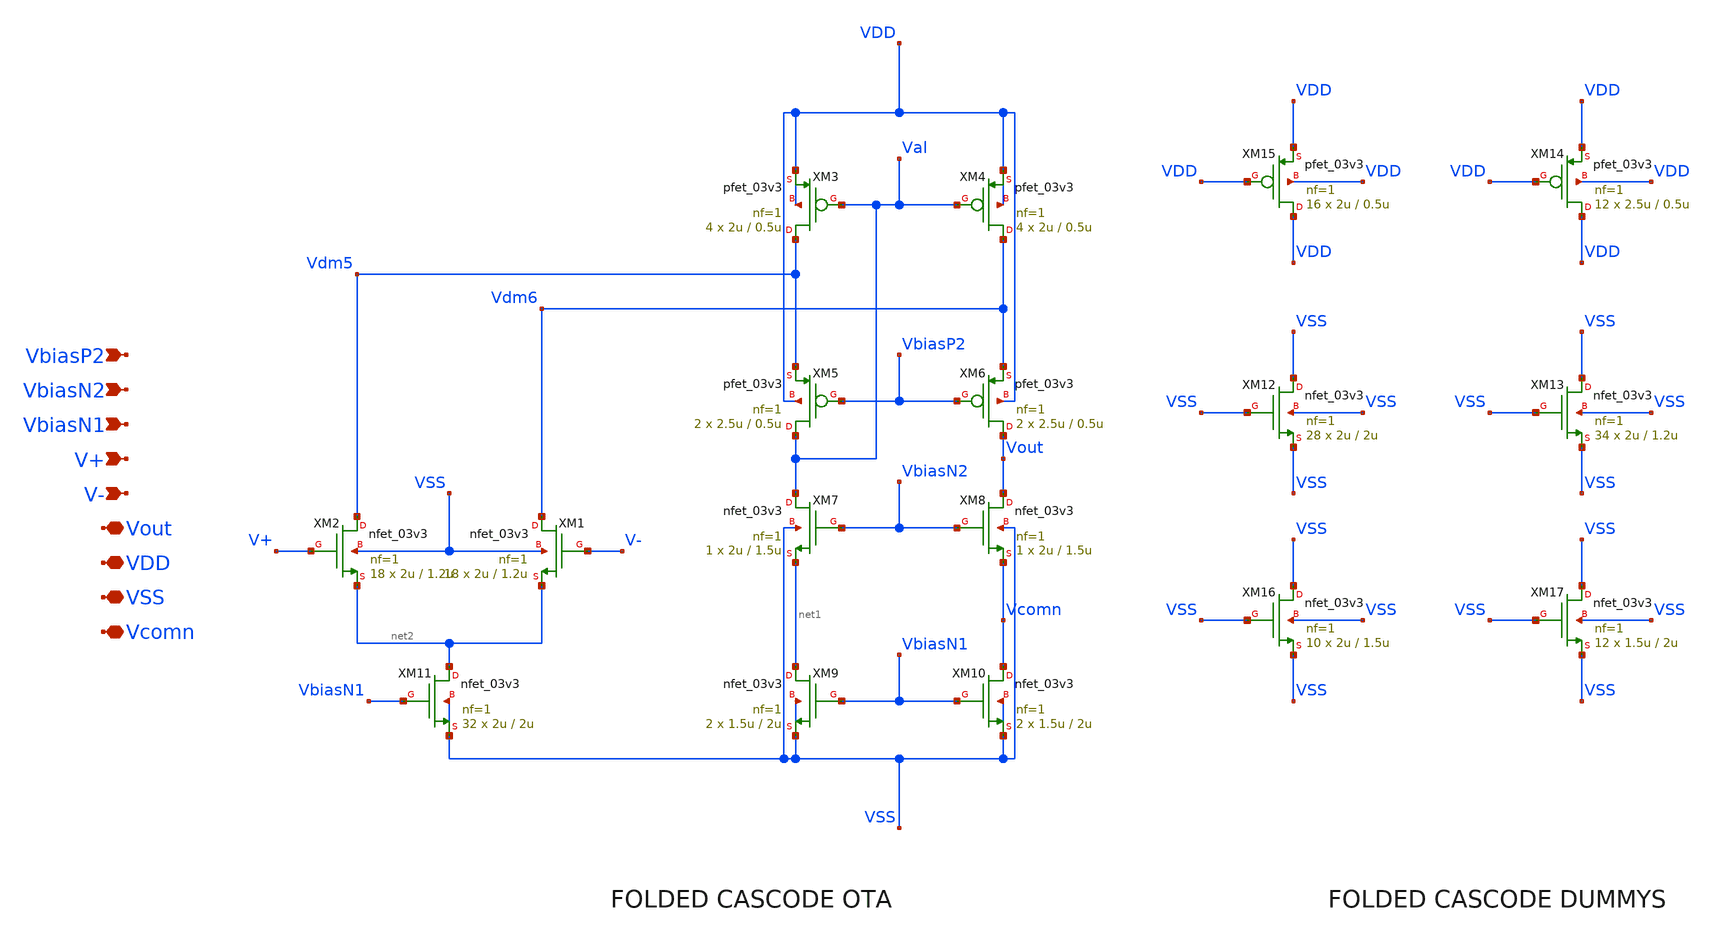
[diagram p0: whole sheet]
** sch_path: designs/gf180/error_amplifier_N_input_core_v3/xschem/error_amplifier_N_input_core_v3.sch
**.subckt error_amplifier_N_input_core_v3 VbiasN2 VDD VbiasP2 VbiasN1 V+ V- VSS Vcomn Vout
*.ipin VbiasN2
*.iopin VDD
*.ipin VbiasP2
*.ipin VbiasN1
*.ipin V+
*.ipin V-
*.iopin VSS
*.iopin Vcomn
*.iopin Vout
XM4 Vdm6 Val VDD VDD pfet_03v3 L=0.5u W=2u nf=1 ad='int((nf+1)/2) * W/nf * 0.18u' as='int((nf+2)/2) * W/nf * 0.18u'
+ pd='2*int((nf+1)/2) * (W/nf + 0.18u)' ps='2*int((nf+2)/2) * (W/nf + 0.18u)' nrd='0.18u / W' nrs='0.18u / W'
+ sa=0 sb=0 sd=0 m=4
XM3 Vdm5 Val VDD VDD pfet_03v3 L=0.5u W=2u nf=1 ad='int((nf+1)/2) * W/nf * 0.18u' as='int((nf+2)/2) * W/nf * 0.18u'
+ pd='2*int((nf+1)/2) * (W/nf + 0.18u)' ps='2*int((nf+2)/2) * (W/nf + 0.18u)' nrd='0.18u / W' nrs='0.18u / W'
+ sa=0 sb=0 sd=0 m=4
XM5 Val VbiasP2 Vdm5 VDD pfet_03v3 L=0.5u W=2.5u nf=1 ad='int((nf+1)/2) * W/nf * 0.18u' as='int((nf+2)/2) * W/nf * 0.18u'
+ pd='2*int((nf+1)/2) * (W/nf + 0.18u)' ps='2*int((nf+2)/2) * (W/nf + 0.18u)' nrd='0.18u / W' nrs='0.18u / W'
+ sa=0 sb=0 sd=0 m=2
XM6 Vout VbiasP2 Vdm6 VDD pfet_03v3 L=0.5u W=2.5u nf=1 ad='int((nf+1)/2) * W/nf * 0.18u' as='int((nf+2)/2) * W/nf * 0.18u'
+ pd='2*int((nf+1)/2) * (W/nf + 0.18u)' ps='2*int((nf+2)/2) * (W/nf + 0.18u)' nrd='0.18u / W' nrs='0.18u / W'
+ sa=0 sb=0 sd=0 m=2
XM9 net1 VbiasN1 VSS VSS nfet_03v3 L=2u W=1.5u nf=1 ad='int((nf+1)/2) * W/nf * 0.18u' as='int((nf+2)/2) * W/nf * 0.18u'
+ pd='2*int((nf+1)/2) * (W/nf + 0.18u)' ps='2*int((nf+2)/2) * (W/nf + 0.18u)' nrd='0.18u / W' nrs='0.18u / W'
+ sa=0 sb=0 sd=0 m=2
XM8 Vout VbiasN2 Vcomn VSS nfet_03v3 L=1.5u W=2u nf=1 ad='int((nf+1)/2) * W/nf * 0.18u' as='int((nf+2)/2) * W/nf * 0.18u'
+ pd='2*int((nf+1)/2) * (W/nf + 0.18u)' ps='2*int((nf+2)/2) * (W/nf + 0.18u)' nrd='0.18u / W' nrs='0.18u / W'
+ sa=0 sb=0 sd=0 m=1
XM7 Val VbiasN2 net1 VSS nfet_03v3 L=1.5u W=2u nf=1 ad='int((nf+1)/2) * W/nf * 0.18u' as='int((nf+2)/2) * W/nf * 0.18u'
+ pd='2*int((nf+1)/2) * (W/nf + 0.18u)' ps='2*int((nf+2)/2) * (W/nf + 0.18u)' nrd='0.18u / W' nrs='0.18u / W'
+ sa=0 sb=0 sd=0 m=1
XM10 Vcomn VbiasN1 VSS VSS nfet_03v3 L=2u W=1.5u nf=1 ad='int((nf+1)/2) * W/nf * 0.18u' as='int((nf+2)/2) * W/nf * 0.18u'
+ pd='2*int((nf+1)/2) * (W/nf + 0.18u)' ps='2*int((nf+2)/2) * (W/nf + 0.18u)' nrd='0.18u / W' nrs='0.18u / W'
+ sa=0 sb=0 sd=0 m=2
XM15 VDD VDD VDD VDD pfet_03v3 L=0.5u W=2u nf=1 ad='int((nf+1)/2) * W/nf * 0.18u' as='int((nf+2)/2) * W/nf * 0.18u'
+ pd='2*int((nf+1)/2) * (W/nf + 0.18u)' ps='2*int((nf+2)/2) * (W/nf + 0.18u)' nrd='0.18u / W' nrs='0.18u / W'
+ sa=0 sb=0 sd=0 m=16
XM13 VSS VSS VSS VSS nfet_03v3 L=1.2u W=2u nf=1 ad='int((nf+1)/2) * W/nf * 0.18u' as='int((nf+2)/2) * W/nf * 0.18u'
+ pd='2*int((nf+1)/2) * (W/nf + 0.18u)' ps='2*int((nf+2)/2) * (W/nf + 0.18u)' nrd='0.18u / W' nrs='0.18u / W'
+ sa=0 sb=0 sd=0 m=34
XM12 VSS VSS VSS VSS nfet_03v3 L=2u W=2u nf=1 ad='int((nf+1)/2) * W/nf * 0.18u' as='int((nf+2)/2) * W/nf * 0.18u'
+ pd='2*int((nf+1)/2) * (W/nf + 0.18u)' ps='2*int((nf+2)/2) * (W/nf + 0.18u)' nrd='0.18u / W' nrs='0.18u / W'
+ sa=0 sb=0 sd=0 m=28
XM1 Vdm6 V- net2 VSS nfet_03v3 L=1.2u W=2u nf=1 ad='int((nf+1)/2) * W/nf * 0.18u' as='int((nf+2)/2) * W/nf * 0.18u'
+ pd='2*int((nf+1)/2) * (W/nf + 0.18u)' ps='2*int((nf+2)/2) * (W/nf + 0.18u)' nrd='0.18u / W' nrs='0.18u / W'
+ sa=0 sb=0 sd=0 m=18
XM2 Vdm5 V+ net2 VSS nfet_03v3 L=1.2u W=2u nf=1 ad='int((nf+1)/2) * W/nf * 0.18u' as='int((nf+2)/2) * W/nf * 0.18u'
+ pd='2*int((nf+1)/2) * (W/nf + 0.18u)' ps='2*int((nf+2)/2) * (W/nf + 0.18u)' nrd='0.18u / W' nrs='0.18u / W'
+ sa=0 sb=0 sd=0 m=18
XM11 net2 VbiasN1 VSS VSS nfet_03v3 L=2u W=2u nf=1 ad='int((nf+1)/2) * W/nf * 0.18u' as='int((nf+2)/2) * W/nf * 0.18u'
+ pd='2*int((nf+1)/2) * (W/nf + 0.18u)' ps='2*int((nf+2)/2) * (W/nf + 0.18u)' nrd='0.18u / W' nrs='0.18u / W'
+ sa=0 sb=0 sd=0 m=32
XM14 VDD VDD VDD VDD pfet_03v3 L=0.5u W=2.5u nf=1 ad='int((nf+1)/2) * W/nf * 0.18u' as='int((nf+2)/2) * W/nf * 0.18u'
+ pd='2*int((nf+1)/2) * (W/nf + 0.18u)' ps='2*int((nf+2)/2) * (W/nf + 0.18u)' nrd='0.18u / W' nrs='0.18u / W'
+ sa=0 sb=0 sd=0 m=12
XM16 VSS VSS VSS VSS nfet_03v3 L=1.5u W=2u nf=1 ad='int((nf+1)/2) * W/nf * 0.18u' as='int((nf+2)/2) * W/nf * 0.18u'
+ pd='2*int((nf+1)/2) * (W/nf + 0.18u)' ps='2*int((nf+2)/2) * (W/nf + 0.18u)' nrd='0.18u / W' nrs='0.18u / W'
+ sa=0 sb=0 sd=0 m=10
XM17 VSS VSS VSS VSS nfet_03v3 L=2u W=1.5u nf=1 ad='int((nf+1)/2) * W/nf * 0.18u' as='int((nf+2)/2) * W/nf * 0.18u'
+ pd='2*int((nf+1)/2) * (W/nf + 0.18u)' ps='2*int((nf+2)/2) * (W/nf + 0.18u)' nrd='0.18u / W' nrs='0.18u / W'
+ sa=0 sb=0 sd=0 m=12
**.ends
.end
